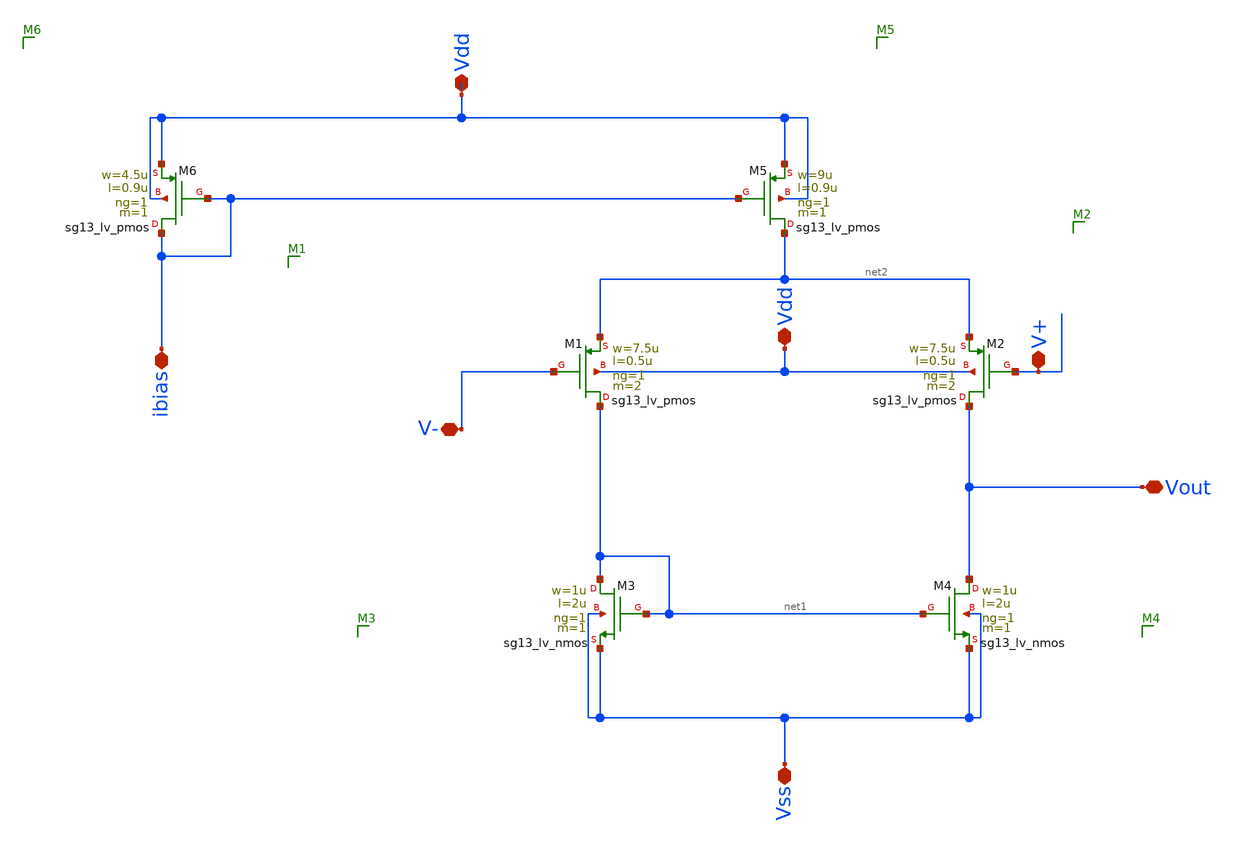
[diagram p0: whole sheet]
** sch_path: Schematics/OTA/ota_sym.sch
**.subckt ota_sym ibias Vdd Vdd Vss V- V+ Vout
*.iopin ibias
*.iopin Vdd
*.iopin Vdd
*.iopin Vss
*.iopin V-
*.iopin V+
*.iopin Vout
XM1 net1 V- net2 Vdd sg13_lv_pmos w=7.5u l=0.5u ng=1 m=2 mm_ok=1
XM2 Vout V+ net2 Vdd sg13_lv_pmos w=7.5u l=0.5u ng=1 m=2 mm_ok=1
XM3 net1 net1 Vss Vss sg13_lv_nmos w=1u l=2u ng=1 m=1 mm_ok=1
XM4 Vout net1 Vss Vss sg13_lv_nmos w=1u l=2u ng=1 m=1 mm_ok=1
XM5 net2 ibias Vdd Vdd sg13_lv_pmos w=9u l=0.9u ng=1 m=1 mm_ok=1
XM6 ibias ibias Vdd Vdd sg13_lv_pmos w=4.5u l=0.9u ng=1 m=1 mm_ok=1
**.ends
.end
